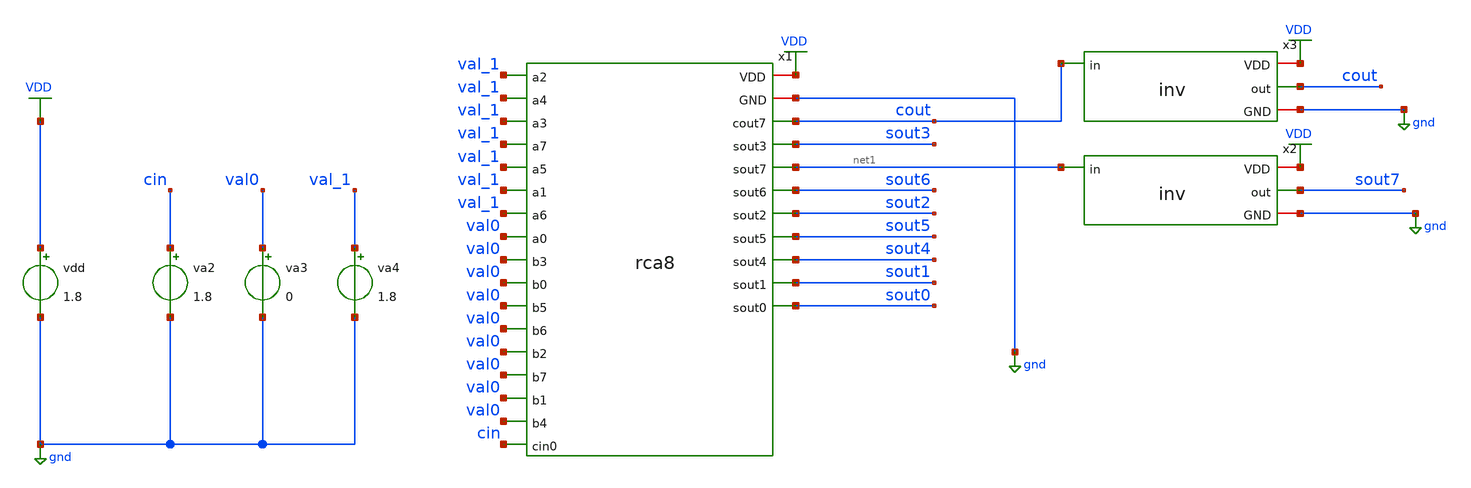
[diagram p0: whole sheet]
** sch_path: assignments/assignment8/assignrca1.sch
**.subckt assignrca1
x1 cout cin val0 val_1 val0 val_1 val0 val_1 val0 val_1 val0 val_1 val0 val_1 val0 val0 val0 val_1
+ sout0 sout1 sout2 sout3 sout4 sout5 sout6 net1 gnd VDD rca8
vdd VDD gnd 1.8
va3 val0 gnd 0
va4 val_1 gnd 1.8
va2 cin gnd 1.8
x2 VDD net1 sout7 gnd inv
x3 VDD cout cout gnd inv
**** begin user architecture code


.control
alter @va2[pulse] = [ 0 1.8 0 10p 10p 4n 8n ]

tran 1p 20n
meas tran delay_cin_net1 TRIG v(cin) VAL=0.9 RISE=3 TARG v(cout) VAL=0.9 FALL=3
plot v(cin) v(sout1)

* Print only the last value for each vector
print v(sout0)[length(v(sout0))-1] v(sout1)[length(v(sout1))-1] v(sout2)[length(v(sout2))-1]
.endc


.lib $::SKYWATER_MODELS/sky130.lib.spice tt
**** end user architecture code
**.ends

* expanding   symbol:  inv.sym # of pins=4
** sym_path: assignments/assignment6/inv.sym
** sch_path: assignments/assignment6/inv.sch
.subckt inv VDD in out GND
*.ipin in
*.iopin GND
*.iopin VDD
*.opin out
XM3 out in GND GND sky130_fd_pr__nfet_01v8 L=0.15 W=0.42 nf=1 ad='int((nf+1)/2) * W/nf * 0.29' as='int((nf+2)/2) * W/nf * 0.29'
+ pd='2*int((nf+1)/2) * (W/nf + 0.29)' ps='2*int((nf+2)/2) * (W/nf + 0.29)' nrd='0.29 / W' nrs='0.29 / W'
+ sa=0 sb=0 sd=0 mult=1 m=1
XM4 out in VDD VDD sky130_fd_pr__pfet_01v8 L=0.15 W=0.84 nf=1 ad='int((nf+1)/2) * W/nf * 0.29' as='int((nf+2)/2) * W/nf * 0.29'
+ pd='2*int((nf+1)/2) * (W/nf + 0.29)' ps='2*int((nf+2)/2) * (W/nf + 0.29)' nrd='0.29 / W' nrs='0.29 / W'
+ sa=0 sb=0 sd=0 mult=1 m=1
.ends

.GLOBAL VDD
.GLOBAL gnd
.end
